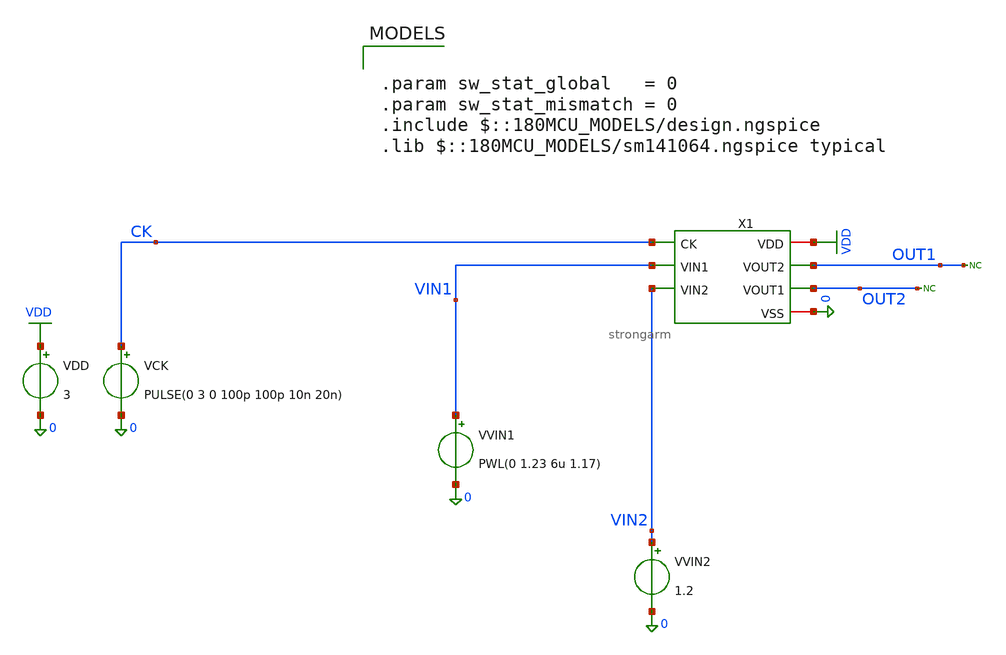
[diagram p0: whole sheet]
** sch_path: comparator/schematic/tests/strongarm_mc_tb_common_mode_test.sch
**.subckt strongarm_mc_tb_common_mode_test
X1 VDD CK OUT1 OUT2 VIN1 VIN2 0 strongarm
VVIN2 VIN2 0 1.2
VVIN1 VIN1 0 PWL(0 1.23 6u 1.17)
VDD VDD 0 3
VCK CK 0 PULSE(0 3 0 100p 100p 10n 20n)
* noconn OUT2
* noconn OUT1
**** begin user architecture code

.param sw_stat_global   = 0
.param sw_stat_mismatch = 0
.include $::180MCU_MODELS/design.ngspice
.lib $::180MCU_MODELS/sm141064.ngspice typical



.control
let mc_runs = 10
set curplotenv = $curplot
unset wr_singlescale

* 1-sigma Vth mismatch per input device (volts).
let svt = 3.0e-3

* common-mode points to test
compose vcm_list values 1.0 1.2 1.4

* storage for the per-VCM results (printed all together at the end)
let mu_list  = vector(length(vcm_list))
let sig_list = vector(length(vcm_list))

let ci = 0
dowhile ci < length(vcm_list)
  let vcm = vcm_list[ci]
  set svcm = $&vcm
  let vlo = vcm - 0.05
  let vhi = vcm + 0.05
  set svlo = $&vlo
  set svhi = $&vhi

  alter vvin2 = $svcm

  let offset_results = vector(mc_runs)
  let run = 0
  echo ########## VCM = $svcm V ##########

  dowhile run < mc_runs
    alter @m.x1.xm10.m0[delvto] = svt * sgauss(0)
    alter @m.x1.xm8.m0[delvto]  = svt * sgauss(0)

    unset s_up
    unset s_dn

    * ---- UP sweep ; trip = LAST fall ----
    alter @vvin1[pwl] = [ 0 $svlo 6e-6 $svhi ]
    tran 10p 6u
    let t_up = -1
    meas tran t_up when v(out1)=1.5 fall=LAST
    if t_up > 0
      meas tran vin_up find v(vin1) at=t_up
      let off_up = vin_up - $svcm
      set s_up = $&off_up
    end
    destroy $curplot

    * ---- DOWN sweep ; trip = FIRST fall ----
    alter @vvin1[pwl] = [ 0 $svhi 6e-6 $svlo ]
    tran 10p 6u
    let t_dn = -1
    meas tran t_dn when v(out1)=1.5 fall=1
    if t_dn > 0
      meas tran vin_dn find v(vin1) at=t_dn
      let off_dn = vin_dn - $svcm
      set s_dn = $&off_dn
    end
    destroy $curplot

    if ( $?s_up * $?s_dn ) = 1
      let offset_results[run] = ( ($s_up) + ($s_dn) ) / 2
    else
      let offset_results[run] = -999
    end

    let run = run + 1
  end

  * ---- stats for this common mode ----
  setplot $curplotenv
  let mu  = mean(offset_results)
  let sig = sqrt(mean((offset_results - mu)^2))
  let mu_list[ci]  = mu
  let sig_list[ci] = sig
  let ci = ci + 1
end

* ===== final summary: all VCM points together, at the very bottom =====
setplot $curplotenv
echo
echo ========== COMMON-MODE SWEEP SUMMARY ==========
let k = 0
dowhile k < length(vcm_list)
  let onev   = vcm_list[k]
  let onemu  = mu_list[k]
  let onesig = sig_list[k]
  echo VCM= $&onev V   systematic= $&onemu V   sigma= $&onesig V
  let k = k + 1
end
echo ===============================================
.endc


**** end user architecture code
**.ends

* expanding   symbol:  comparator/schematic/strongarm.sym # of pins=7
** sym_path: comparator/schematic/strongarm.sym
** sch_path: comparator/schematic/strongarm.sch
.subckt strongarm VDD CK VOUT2 VOUT1 VIN1 VIN2 VSS
*.opin VOUT1
*.opin VOUT2
*.ipin VIN1
*.ipin VIN2
*.ipin CK
*.iopin VDD
*.iopin VSS
XM1 VOUT2 VOUT1 net1 net1 nfet_03v3 L=0.28u W=0.22u nf=1 ad='int((nf+1)/2) * W/nf * 0.18u' as='int((nf+2)/2) * W/nf * 0.18u'
+ pd='2*int((nf+1)/2) * (W/nf + 0.18u)' ps='2*int((nf+2)/2) * (W/nf + 0.18u)' nrd='0.18u / W' nrs='0.18u / W'
+ sa=0 sb=0 sd=0 m=1
XM2 VOUT1 VOUT2 VDD VDD pfet_03v3 L=0.28u W=0.22u nf=1 ad='int((nf+1)/2) * W/nf * 0.18u' as='int((nf+2)/2) * W/nf * 0.18u'
+ pd='2*int((nf+1)/2) * (W/nf + 0.18u)' ps='2*int((nf+2)/2) * (W/nf + 0.18u)' nrd='0.18u / W' nrs='0.18u / W'
+ sa=0 sb=0 sd=0 m=1
XM3 VOUT1 CK VDD VDD pfet_03v3 L=0.28u W=0.22u nf=1 ad='int((nf+1)/2) * W/nf * 0.18u' as='int((nf+2)/2) * W/nf * 0.18u'
+ pd='2*int((nf+1)/2) * (W/nf + 0.18u)' ps='2*int((nf+2)/2) * (W/nf + 0.18u)' nrd='0.18u / W' nrs='0.18u / W'
+ sa=0 sb=0 sd=0 m=1
XM4 net3 CK VDD VDD pfet_03v3 L=0.28u W=0.22u nf=1 ad='int((nf+1)/2) * W/nf * 0.18u' as='int((nf+2)/2) * W/nf * 0.18u'
+ pd='2*int((nf+1)/2) * (W/nf + 0.18u)' ps='2*int((nf+2)/2) * (W/nf + 0.18u)' nrd='0.18u / W' nrs='0.18u / W'
+ sa=0 sb=0 sd=0 m=1
XM5 net1 CK VDD VDD pfet_03v3 L=0.28u W=0.22u nf=1 ad='int((nf+1)/2) * W/nf * 0.18u' as='int((nf+2)/2) * W/nf * 0.18u'
+ pd='2*int((nf+1)/2) * (W/nf + 0.18u)' ps='2*int((nf+2)/2) * (W/nf + 0.18u)' nrd='0.18u / W' nrs='0.18u / W'
+ sa=0 sb=0 sd=0 m=1
XM6 VOUT2 CK VDD VDD pfet_03v3 L=0.28u W=0.22u nf=1 ad='int((nf+1)/2) * W/nf * 0.18u' as='int((nf+2)/2) * W/nf * 0.18u'
+ pd='2*int((nf+1)/2) * (W/nf + 0.18u)' ps='2*int((nf+2)/2) * (W/nf + 0.18u)' nrd='0.18u / W' nrs='0.18u / W'
+ sa=0 sb=0 sd=0 m=1
XM7 VOUT2 VOUT1 VDD VDD pfet_03v3 L=0.28u W=0.22u nf=1 ad='int((nf+1)/2) * W/nf * 0.18u' as='int((nf+2)/2) * W/nf * 0.18u'
+ pd='2*int((nf+1)/2) * (W/nf + 0.18u)' ps='2*int((nf+2)/2) * (W/nf + 0.18u)' nrd='0.18u / W' nrs='0.18u / W'
+ sa=0 sb=0 sd=0 m=1
XM8 net1 VIN2 net2 net2 nfet_03v3 L=0.28u W=0.22u nf=1 ad='int((nf+1)/2) * W/nf * 0.18u' as='int((nf+2)/2) * W/nf * 0.18u'
+ pd='2*int((nf+1)/2) * (W/nf + 0.18u)' ps='2*int((nf+2)/2) * (W/nf + 0.18u)' nrd='0.18u / W' nrs='0.18u / W'
+ sa=0 sb=0 sd=0 m=1
XM9 VOUT1 VOUT2 net3 net3 nfet_03v3 L=0.28u W=0.22u nf=1 ad='int((nf+1)/2) * W/nf * 0.18u' as='int((nf+2)/2) * W/nf * 0.18u'
+ pd='2*int((nf+1)/2) * (W/nf + 0.18u)' ps='2*int((nf+2)/2) * (W/nf + 0.18u)' nrd='0.18u / W' nrs='0.18u / W'
+ sa=0 sb=0 sd=0 m=1
XM10 net3 VIN1 net2 net2 nfet_03v3 L=0.28u W=0.22u nf=1 ad='int((nf+1)/2) * W/nf * 0.18u' as='int((nf+2)/2) * W/nf * 0.18u'
+ pd='2*int((nf+1)/2) * (W/nf + 0.18u)' ps='2*int((nf+2)/2) * (W/nf + 0.18u)' nrd='0.18u / W' nrs='0.18u / W'
+ sa=0 sb=0 sd=0 m=1
XM11 net2 CK VSS net2 nfet_03v3 L=0.28u W=0.22u nf=1 ad='int((nf+1)/2) * W/nf * 0.18u' as='int((nf+2)/2) * W/nf * 0.18u'
+ pd='2*int((nf+1)/2) * (W/nf + 0.18u)' ps='2*int((nf+2)/2) * (W/nf + 0.18u)' nrd='0.18u / W' nrs='0.18u / W'
+ sa=0 sb=0 sd=0 m=1
.ends

.GLOBAL VDD
.end
